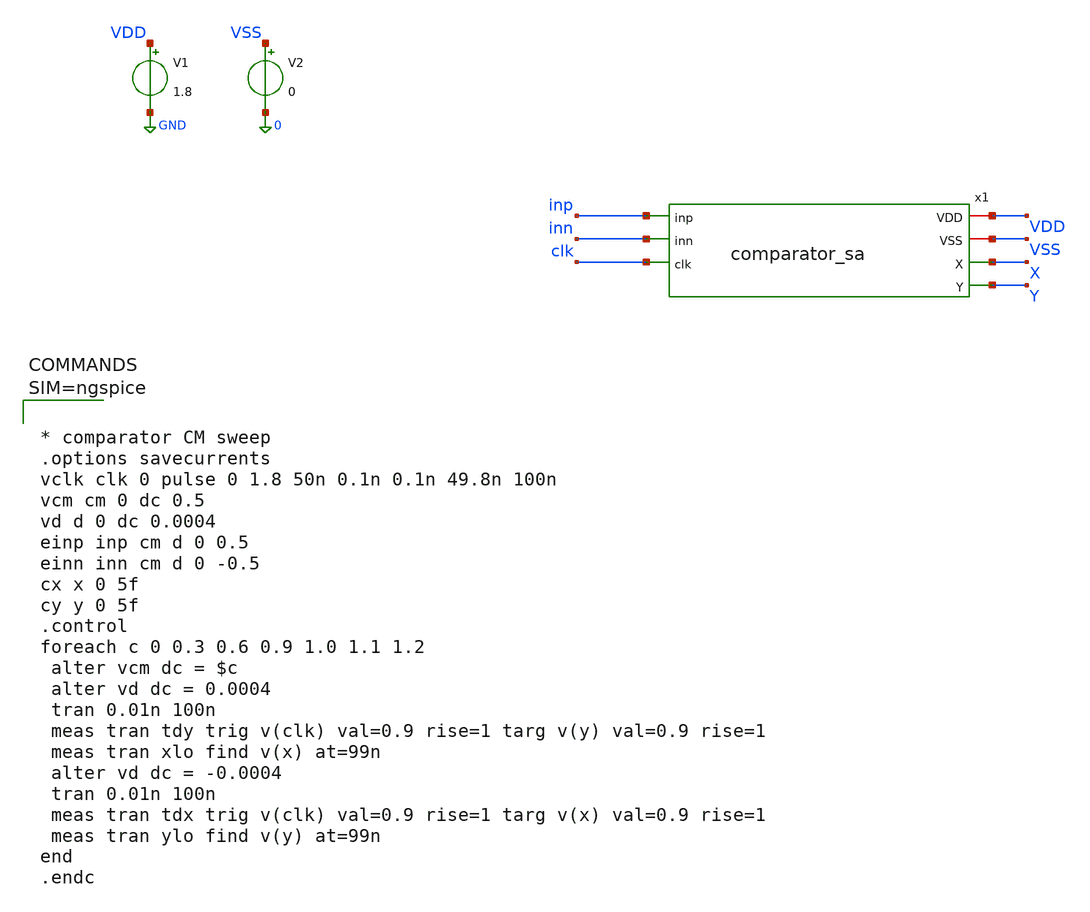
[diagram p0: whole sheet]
** sch_path: xschem/comparator_sa_tb.sch
**.subckt comparator_sa_tb
V1 VDD GND 1.8
V2 VSS 0 0
x1 inp VDD inn clk VSS X Y comparator_sa
**** begin user architecture code

** opencircuitdesign pdks install
.lib $::SKYWATER_MODELS/sky130.lib.spice tt




* comparator CM sweep
.options savecurrents
vclk clk 0 pulse 0 1.8 50n 0.1n 0.1n 49.8n 100n
vcm cm 0 dc 0.5
vd d 0 dc 0.0004
einp inp cm d 0 0.5
einn inn cm d 0 -0.5
cx x 0 5f
cy y 0 5f
.control
foreach c 0 0.3 0.6 0.9 1.0 1.1 1.2
 alter vcm dc = $c
 alter vd dc = 0.0004
 tran 0.01n 100n
 meas tran tdy trig v(clk) val=0.9 rise=1 targ v(y) val=0.9 rise=1
 meas tran xlo find v(x) at=99n
 alter vd dc = -0.0004
 tran 0.01n 100n
 meas tran tdx trig v(clk) val=0.9 rise=1 targ v(x) val=0.9 rise=1
 meas tran ylo find v(y) at=99n
end
.endc



**** end user architecture code
**.ends

* expanding   symbol:  comparator_sa.sym # of pins=7
** sym_path: xschem/comparator_sa.sym
** sch_path: xschem/comparator_sa.sch
.subckt comparator_sa inp VDD inn clk VSS X Y
*.ipin inp
*.ipin inn
*.ipin clk
*.opin X
*.opin Y
*.iopin VDD
*.iopin VSS
XM7 T ckb VDD VDD sky130_fd_pr__pfet_01v8 L=0.15 W=4 nf=1 ad='int((1 + 1)/2) * 4 / 1 * 0.29' as='int((1 + 2)/2) * 4 / 1 * 0.29'
+ pd='2*int((1 + 1)/2) * (4 / 1 + 0.29)' ps='2*int((1 + 2)/2) * (4 / 1 + 0.29)' nrd='0.29 / 4 ' nrs='0.29 / 4 '
+ sa=0 sb=0 sd=0 mult=1 m=1
XM1 P inp T T sky130_fd_pr__pfet_01v8_lvt L=0.5 W=8 nf=4 ad='int((4 + 1)/2) * 8 / 4 * 0.29' as='int((4 + 2)/2) * 8 / 4 * 0.29'
+ pd='2*int((4 + 1)/2) * (8 / 4 + 0.29)' ps='2*int((4 + 2)/2) * (8 / 4 + 0.29)' nrd='0.29 / 8 ' nrs='0.29 / 8 '
+ sa=0 sb=0 sd=0 mult=1 m=1
XM2 Q inn T T sky130_fd_pr__pfet_01v8_lvt L=0.5 W=8 nf=4 ad='int((4 + 1)/2) * 8 / 4 * 0.29' as='int((4 + 2)/2) * 8 / 4 * 0.29'
+ pd='2*int((4 + 1)/2) * (8 / 4 + 0.29)' ps='2*int((4 + 2)/2) * (8 / 4 + 0.29)' nrd='0.29 / 8 ' nrs='0.29 / 8 '
+ sa=0 sb=0 sd=0 mult=1 m=1
XM3 X Y P VDD sky130_fd_pr__pfet_01v8 L=0.15 W=2 nf=1 ad='int((1 + 1)/2) * 2 / 1 * 0.29' as='int((1 + 2)/2) * 2 / 1 * 0.29'
+ pd='2*int((1 + 1)/2) * (2 / 1 + 0.29)' ps='2*int((1 + 2)/2) * (2 / 1 + 0.29)' nrd='0.29 / 2 ' nrs='0.29 / 2 '
+ sa=0 sb=0 sd=0 mult=1 m=1
XM4 Y X Q VDD sky130_fd_pr__pfet_01v8 L=0.15 W=2 nf=1 ad='int((1 + 1)/2) * 2 / 1 * 0.29' as='int((1 + 2)/2) * 2 / 1 * 0.29'
+ pd='2*int((1 + 1)/2) * (2 / 1 + 0.29)' ps='2*int((1 + 2)/2) * (2 / 1 + 0.29)' nrd='0.29 / 2 ' nrs='0.29 / 2 '
+ sa=0 sb=0 sd=0 mult=1 m=1
XM6 Y X VSS VSS sky130_fd_pr__nfet_01v8 L=0.15 W=1 nf=1 ad='int((1 + 1)/2) * 1 / 1 * 0.29' as='int((1 + 2)/2) * 1 / 1 * 0.29'
+ pd='2*int((1 + 1)/2) * (1 / 1 + 0.29)' ps='2*int((1 + 2)/2) * (1 / 1 + 0.29)' nrd='0.29 / 1 ' nrs='0.29 / 1 '
+ sa=0 sb=0 sd=0 mult=1 m=1
XM5 X Y VSS VSS sky130_fd_pr__nfet_01v8 L=0.15 W=1 nf=1 ad='int((1 + 1)/2) * 1 / 1 * 0.29' as='int((1 + 2)/2) * 1 / 1 * 0.29'
+ pd='2*int((1 + 1)/2) * (1 / 1 + 0.29)' ps='2*int((1 + 2)/2) * (1 / 1 + 0.29)' nrd='0.29 / 1 ' nrs='0.29 / 1 '
+ sa=0 sb=0 sd=0 mult=1 m=1
XS4 Y ckb VSS VSS sky130_fd_pr__nfet_01v8 L=0.15 W=0.5 nf=1 ad='int((1 + 1)/2) * 0.5 / 1 * 0.29' as='int((1 + 2)/2) * 0.5 / 1 * 0.29'
+ pd='2*int((1 + 1)/2) * (0.5 / 1 + 0.29)' ps='2*int((1 + 2)/2) * (0.5 / 1 + 0.29)' nrd='0.29 / 0.5 ' nrs='0.29 / 0.5 '
+ sa=0 sb=0 sd=0 mult=1 m=1
XS2 Q ckb VSS VSS sky130_fd_pr__nfet_01v8 L=0.15 W=0.5 nf=1 ad='int((1 + 1)/2) * 0.5 / 1 * 0.29' as='int((1 + 2)/2) * 0.5 / 1 * 0.29'
+ pd='2*int((1 + 1)/2) * (0.5 / 1 + 0.29)' ps='2*int((1 + 2)/2) * (0.5 / 1 + 0.29)' nrd='0.29 / 0.5 ' nrs='0.29 / 0.5 '
+ sa=0 sb=0 sd=0 mult=1 m=1
XS3 X ckb VSS VSS sky130_fd_pr__nfet_01v8 L=0.15 W=0.5 nf=1 ad='int((1 + 1)/2) * 0.5 / 1 * 0.29' as='int((1 + 2)/2) * 0.5 / 1 * 0.29'
+ pd='2*int((1 + 1)/2) * (0.5 / 1 + 0.29)' ps='2*int((1 + 2)/2) * (0.5 / 1 + 0.29)' nrd='0.29 / 0.5 ' nrs='0.29 / 0.5 '
+ sa=0 sb=0 sd=0 mult=1 m=1
XS1 P ckb VSS VSS sky130_fd_pr__nfet_01v8 L=0.15 W=0.5 nf=1 ad='int((1 + 1)/2) * 0.5 / 1 * 0.29' as='int((1 + 2)/2) * 0.5 / 1 * 0.29'
+ pd='2*int((1 + 1)/2) * (0.5 / 1 + 0.29)' ps='2*int((1 + 2)/2) * (0.5 / 1 + 0.29)' nrd='0.29 / 0.5 ' nrs='0.29 / 0.5 '
+ sa=0 sb=0 sd=0 mult=1 m=1
XMIN ckb clk VSS VSS sky130_fd_pr__nfet_01v8 L=0.15 W=1 nf=1 ad='int((1 + 1)/2) * 1 / 1 * 0.29' as='int((1 + 2)/2) * 1 / 1 * 0.29'
+ pd='2*int((1 + 1)/2) * (1 / 1 + 0.29)' ps='2*int((1 + 2)/2) * (1 / 1 + 0.29)' nrd='0.29 / 1 ' nrs='0.29 / 1 '
+ sa=0 sb=0 sd=0 mult=1 m=1
XMIP ckb clk VDD VDD sky130_fd_pr__pfet_01v8 L=0.15 W=2 nf=1 ad='int((1 + 1)/2) * 2 / 1 * 0.29' as='int((1 + 2)/2) * 2 / 1 * 0.29'
+ pd='2*int((1 + 1)/2) * (2 / 1 + 0.29)' ps='2*int((1 + 2)/2) * (2 / 1 + 0.29)' nrd='0.29 / 2 ' nrs='0.29 / 2 '
+ sa=0 sb=0 sd=0 mult=1 m=1
.ends

.GLOBAL GND
.end
